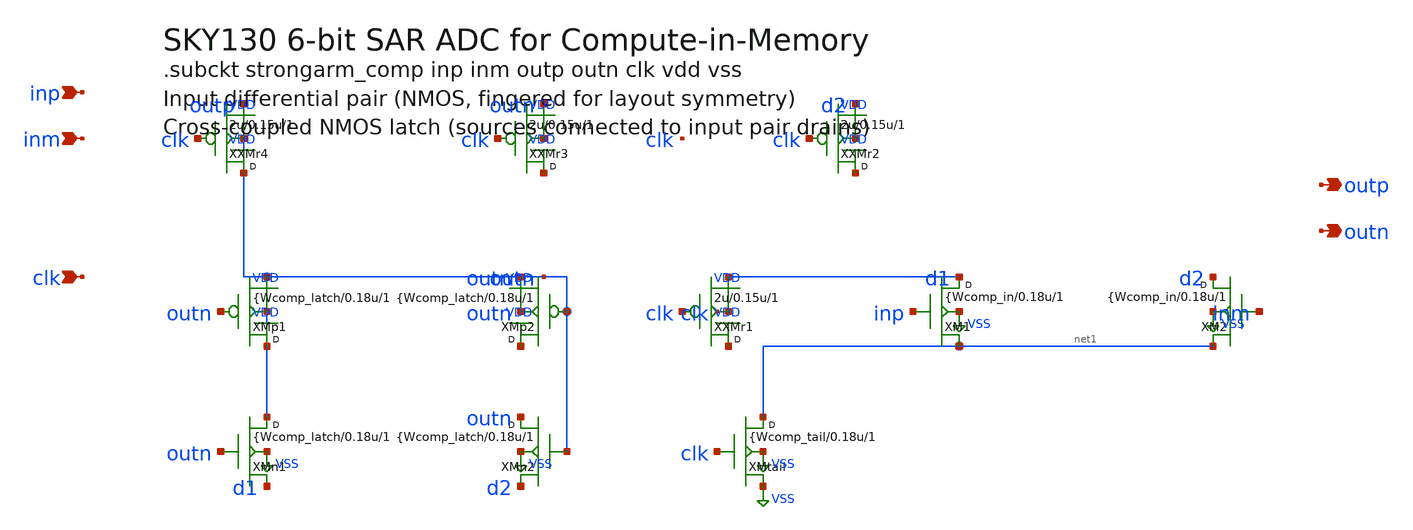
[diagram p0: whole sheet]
** sch_path: data/sch/cim_adc.sch
**.subckt cim_adc inp inm outp outn clk
*.ipin inp
*.ipin inm
*.opin outp
*.opin outn
*.ipin clk
XMtail net1 clk VSS VSS nmos w={Wcomp_tail l=0.18u m=1
XM1 d1 inp net1 VSS nmos w={Wcomp_in l=0.18u m=1
XM2 d2 inm net1 VSS nmos w={Wcomp_in l=0.18u m=1
XXMr1 VDD clk d1 VDD sky130_fd_pr__pfet_01v8 w=2u l=0.15u m=1
XXMr2 VDD clk d2 VDD sky130_fd_pr__pfet_01v8 w=2u l=0.15u m=1
XXMr3 VDD clk outn VDD sky130_fd_pr__pfet_01v8 w=2u l=0.15u m=1
XXMr4 VDD clk VDD VDD sky130_fd_pr__pfet_01v8 w=2u l=0.15u m=1
XMp1 VDD outn VDD VDD pmos w={Wcomp_latch l=0.18u m=1
XMp2 VDD VDD VDD VDD pmos w={Wcomp_latch l=0.18u m=1
XMn1 VDD outn d1 VSS nmos w={Wcomp_latch l=0.18u m=1
XMn2 outn VDD d2 VSS nmos w={Wcomp_latch l=0.18u m=1
**.ends
.GLOBAL VSS
.GLOBAL VDD
.end
